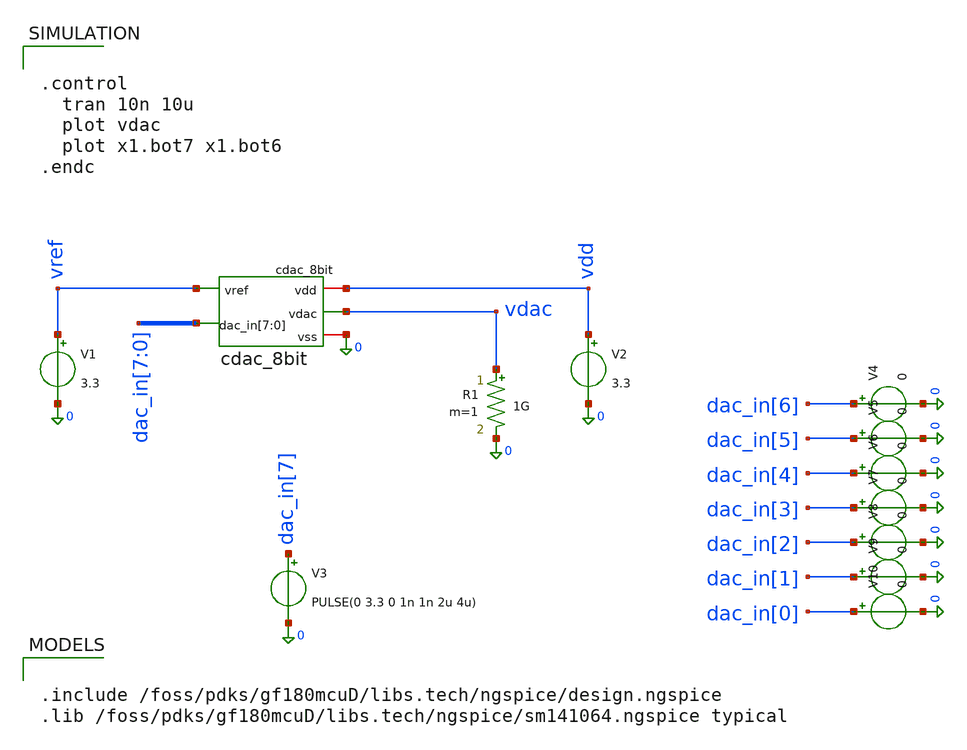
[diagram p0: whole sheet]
** sch_path: xschem/sar_adc/blocks/cdac/testbench/tb_cdac_8bit.sch
**.subckt tb_cdac_8bit
V1 vref 0 3.3
V2 vdd 0 3.3
R1 vdac 0 1G m=1
V3 dac_in[7] 0 PULSE(0 3.3 0 1n 1n 2u 4u)
V4 dac_in[6] 0 0
V5 dac_in[5] 0 0
V6 dac_in[4] 0 0
V7 dac_in[3] 0 0
V8 dac_in[2] 0 0
V9 dac_in[1] 0 0
V10 dac_in[0] 0 0
x1 vref vdd 0 dac_in[7] dac_in[6] dac_in[5] dac_in[4] dac_in[3] dac_in[2] dac_in[1] dac_in[0] vdac
+ cdac_8bit
**** begin user architecture code


.include /foss/pdks/gf180mcuD/libs.tech/ngspice/design.ngspice
.lib /foss/pdks/gf180mcuD/libs.tech/ngspice/sm141064.ngspice typical




.control
  tran 10n 10u
  plot vdac
  plot x1.bot7 x1.bot6
.endc


**** end user architecture code
**.ends

* expanding   symbol:  sar_adc/blocks/cdac/cdac_8bit.sym # of pins=5
** sym_path: xschem/sar_adc/blocks/cdac/cdac_8bit.sym
** sch_path: xschem/sar_adc/blocks/cdac/cdac_8bit.sch
.subckt cdac_8bit vref vdd vss dac_in[7] dac_in[6] dac_in[5] dac_in[4] dac_in[3] dac_in[2] dac_in[1]
+ dac_in[0] vdac
*.ipin vref
*.iopin vdd
*.iopin vss
*.opin vdac
*.ipin dac_in[7],dac_in[6],dac_in[5],dac_in[4],dac_in[3],dac_in[2],dac_in[1],dac_in[0]
C0 vdac bot0 0.01p m=1
C1 vdac bot1 0.02p m=1
C2 vdac bot2 0.04p m=1
C3 vdac bot3 0.08p m=1
C4 vdac bot4 0.16p m=1
C5 vdac bot5 0.32p m=1
C6 vdac bot6 0.64p m=1
C7 vdac bot7 1.28p m=1
XSW0 vref vdd vss bot0 dac_in[0] cdac_switch_1b
XSW1 vref vdd vss bot1 dac_in[1] cdac_switch_1b
XSW2 vref vdd vss bot2 dac_in[2] cdac_switch_1b
XSW3 vref vdd vss bot3 dac_in[3] cdac_switch_1b
XSW4 vref vdd vss bot4 dac_in[4] cdac_switch_1b
XSW5 vref vdd vss bot5 dac_in[5] cdac_switch_1b
XSW6 vref vdd vss bot6 dac_in[6] cdac_switch_1b
XSW7 vref vdd vss bot7 dac_in[7] cdac_switch_1b
CDummy vdac vss 0.01p m=1
.ends


* expanding   symbol:  sar_adc/blocks/cdac/cdac_switch_1b.sym # of pins=5
** sym_path: xschem/sar_adc/blocks/cdac/cdac_switch_1b.sym
** sch_path: xschem/sar_adc/blocks/cdac/cdac_switch_1b.sch
.subckt cdac_switch_1b vref vdd vss bot bit
*.iopin vdd
*.iopin vss
*.iopin vref
*.ipin bit
*.iopin bot
XM1 bit_b bit vdd vdd pfet_03v3 L=0.28u W=1u nf=1 ad='int((nf+1)/2) * W/nf * 0.18u' as='int((nf+2)/2) * W/nf * 0.18u'
+ pd='2*int((nf+1)/2) * (W/nf + 0.18u)' ps='2*int((nf+2)/2) * (W/nf + 0.18u)' nrd='0.18u / W' nrs='0.18u / W'
+ sa=0 sb=0 sd=0 m=1
XM2 bit_b bit vss vss nfet_03v3 L=0.28u W=0.5u nf=1 ad='int((nf+1)/2) * W/nf * 0.18u' as='int((nf+2)/2) * W/nf * 0.18u'
+ pd='2*int((nf+1)/2) * (W/nf + 0.18u)' ps='2*int((nf+2)/2) * (W/nf + 0.18u)' nrd='0.18u / W' nrs='0.18u / W'
+ sa=0 sb=0 sd=0 m=1
XM3 bot bit_b vref vdd pfet_03v3 L=0.28u W=4u nf=1 ad='int((nf+1)/2) * W/nf * 0.18u' as='int((nf+2)/2) * W/nf * 0.18u'
+ pd='2*int((nf+1)/2) * (W/nf + 0.18u)' ps='2*int((nf+2)/2) * (W/nf + 0.18u)' nrd='0.18u / W' nrs='0.18u / W'
+ sa=0 sb=0 sd=0 m=1
XM4 vref bit bot vss nfet_03v3 L=0.28u W=2u nf=1 ad='int((nf+1)/2) * W/nf * 0.18u' as='int((nf+2)/2) * W/nf * 0.18u'
+ pd='2*int((nf+1)/2) * (W/nf + 0.18u)' ps='2*int((nf+2)/2) * (W/nf + 0.18u)' nrd='0.18u / W' nrs='0.18u / W'
+ sa=0 sb=0 sd=0 m=1
XM5 bot bit vss vdd pfet_03v3 L=0.28u W=4u nf=1 ad='int((nf+1)/2) * W/nf * 0.18u' as='int((nf+2)/2) * W/nf * 0.18u'
+ pd='2*int((nf+1)/2) * (W/nf + 0.18u)' ps='2*int((nf+2)/2) * (W/nf + 0.18u)' nrd='0.18u / W' nrs='0.18u / W'
+ sa=0 sb=0 sd=0 m=1
XM6 vss bit_b bot vss nfet_03v3 L=0.28u W=2u nf=1 ad='int((nf+1)/2) * W/nf * 0.18u' as='int((nf+2)/2) * W/nf * 0.18u'
+ pd='2*int((nf+1)/2) * (W/nf + 0.18u)' ps='2*int((nf+2)/2) * (W/nf + 0.18u)' nrd='0.18u / W' nrs='0.18u / W'
+ sa=0 sb=0 sd=0 m=1
.ends

.end
